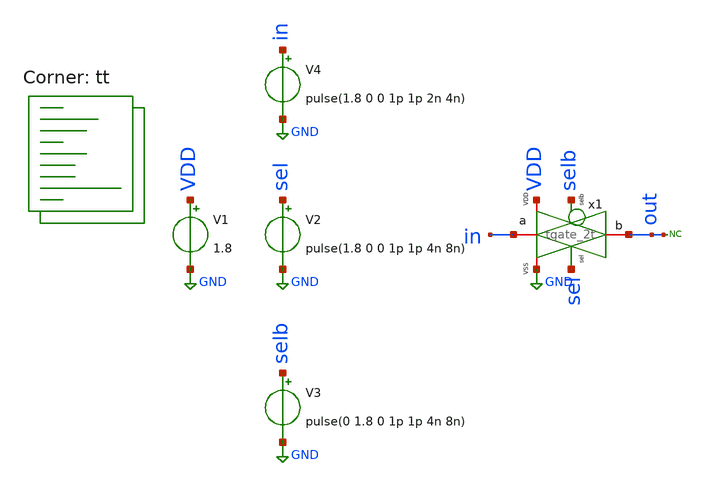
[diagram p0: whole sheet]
** sch_path: xsch/tb/tgate/2t/tgate_2t_tb.sch
**.subckt tgate_2t_tb
x1 VDD GND in out sel selb tgate_2t
V1 VDD GND 1.8
V2 sel GND pulse(1.8 0 0 1p 1p 4n 8n)
V3 selb GND pulse(0 1.8 0 1p 1p 4n 8n)
V4 in GND pulse(1.8 0 0 1p 1p 2n 4n)
* noconn out
**** begin user architecture code
.lib $::SKYWATER_MODELS/sky130.lib.spice tt



.control
save v(in) v(out) v(sel) v(selb)
tran 1p 10n
write tgate_2t_tran.raw
quit
.endc


**** end user architecture code
**.ends

* expanding   symbol:  ip/tgate/tgate_2t.sym # of pins=6
** sym_path: xsch/ip/tgate/tgate_2t.sym
** sch_path: xsch/ip/tgate/tgate_2t.sch
.subckt tgate_2t VDD VSS a b sel selb
*.iopin a
*.iopin b
*.iopin VDD
*.iopin VSS
*.ipin sel
*.ipin selb
XM4 a selb b VDD sky130_fd_pr__pfet_01v8 L=0.15 W=2 nf=1 ad='int((nf+1)/2) * W/nf * 0.29' as='int((nf+2)/2) * W/nf * 0.29'
+ pd='2*int((nf+1)/2) * (W/nf + 0.29)' ps='2*int((nf+2)/2) * (W/nf + 0.29)' nrd='0.29 / W' nrs='0.29 / W'
+ sa=0 sb=0 sd=0 mult=1 m=1
XM5 a sel b VSS sky130_fd_pr__nfet_01v8 L=0.15 W=1 nf=1 ad='int((1 + 1)/2) * 1 / 1 * 0.29' as='int((1 + 2)/2) * 1 / 1 * 0.29'
+ pd='2*int((1 + 1)/2) * (1 / 1 + 0.29)' ps='2*int((1 + 2)/2) * (1 / 1 + 0.29)' nrd='0.29 / 1 ' nrs='0.29 / 1 '
+ sa=0 sb=0 sd=0 mult=1 m=1
.ends

.GLOBAL GND
.end
